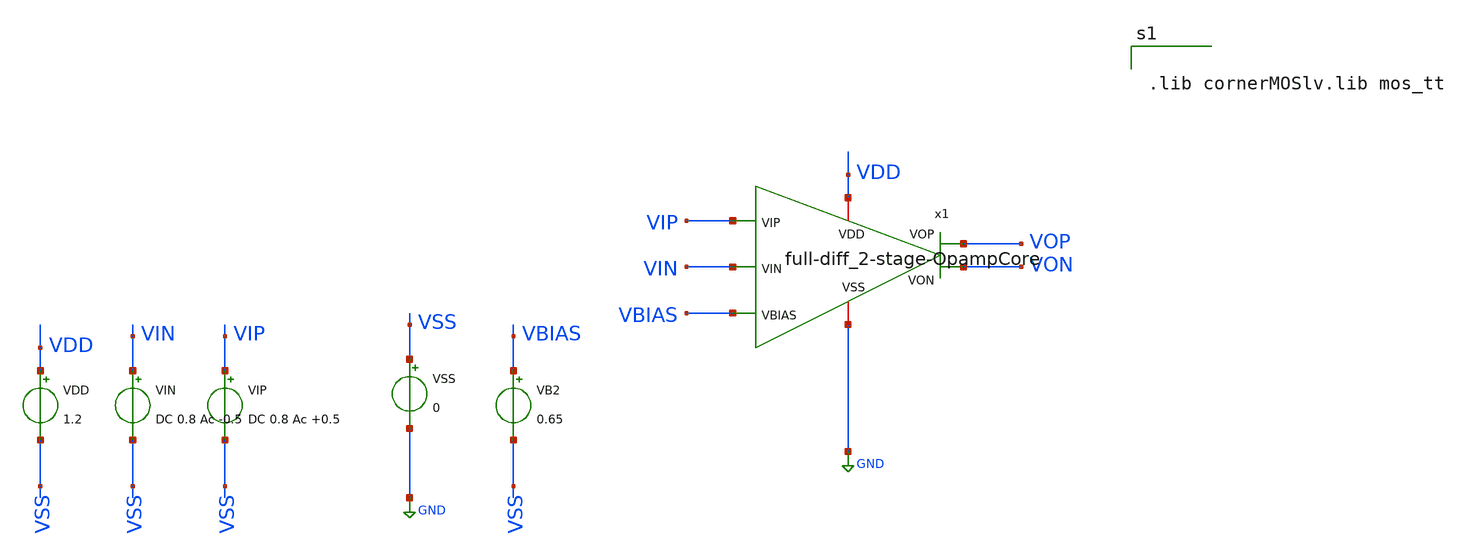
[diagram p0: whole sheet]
** sch_path: BTDay5-Ex/Test-diff_2stageOpampCore.sch
**.subckt Test-diff_2stageOpampCore
VDD VDD VSS 1.2
VIN VIN VSS DC 0.8 Ac -0.5
VIP VIP VSS DC 0.8 Ac +0.5
VSS VSS GND 0
VB2 VBIAS VSS 0.65
x1 VDD VBIAS VOP VON VIP VIN GND full-diff_2-stage-OpampCore
**** begin user architecture code


.lib cornerMOSlv.lib mos_tt




.control
save all
op

* 1. DO CONG SUAT VA DIEM LAM VIEC DC
let power_mw = abs(i(vdd)[0]) * 1.2 * 1000
echo ================= KET QUA DC & CONG SUAT =================
print v(vip) v(vin) v(vbias) v(vop) v(von)
print power_mw

* 2. MO PHONG AC VA TINH TOAN HE SO
ac dec 100 1 10G

let vid = v(vip) - v(vin)
let vod = v(vop) - v(von)
let av = vod / vid
let gain_db = db(av)
let phase_deg = cph(av) * 180 / pi

* Do Open Loop Gain o tan so thap (dang so lan)
let open_loop_gain_times = mag(av[0])

if phase_deg[0] > 90
  let phase_deg = phase_deg - 360
end

* Do tan so cat 0dB va Phase Margin
meas ac f_ug when gain_db=0 fall=1
meas ac phase_at_ug find phase_deg when gain_db=0 fall=1
let phase_margin = 180 + phase_at_ug

echo ================= TONG HOP CHI TIEU EX2 =================
echo 1. Open Loop Gain (Yeu cau: > 3000):
print open_loop_gain_times
echo 2. DC Gain dB (Yeu cau: > 50 dB):
print gain_db[0]
echo 3. Bandwidth GBW f_ug (Yeu cau: > 3 MHz):
print f_ug
echo 4. Phase Margin (Yeu cau: 50 - 60 deg):
print phase_margin
echo 5. Cong suat Power (Yeu cau: < 2 mW):
print power_mw
echo =========================================================

let line_0db = 0 * frequency
let line_m180 = -180 + 0 * frequency

plot gain_db phase_deg line_0db line_m180 xlog ylimit -360 80 title 'Ex2: Fully-Diff OpAmp Open-Loop Frequency Response'
.endc


**** end user architecture code
**.ends

* expanding   symbol:  /foss/designs/BTDay5-Ex/full-diff_2-stage-OpampCore.sym # of pins=7
** sym_path: BTDay5-Ex/full-diff_2-stage-OpampCore.sym
** sch_path: BTDay5-Ex/full-diff_2-stage-OpampCore.sch
.subckt full-diff_2-stage-OpampCore VDD VBIAS VOP VON VIP VIN VSS
*.ipin VIN
*.ipin VIP
*.opin VOP
*.iopin VDD
*.iopin VSS
*.ipin VBIAS
*.opin VON
XM1 net3 VIN net1 VSS sg13_lv_nmos w=4u l=1u ng=1 m=2 mm_ok=1
XM2 net2 VIP net1 VSS sg13_lv_nmos w=4u l=1u ng=1 m=2 mm_ok=1
XM3 net1 VB2 VSS VSS sg13_lv_nmos w=4u l=1u ng=1 m=4 mm_ok=1
XM4 net3 VB1 VDD VDD sg13_lv_pmos w=8u l=1u ng=1 m=2 mm_ok=1
XM7 VB2 VB2 VSS VSS sg13_lv_nmos w=4u l=1u ng=1 m=1 mm_ok=1
XM8 VB2 VBIAS VDD VDD sg13_lv_pmos w=2u l=6u ng=1 m=1 mm_ok=1
XM10 net2 VB1 VDD VDD sg13_lv_pmos w=8u l=1u ng=1 m=2 mm_ok=1
XM5 VOP VB2 VSS VSS sg13_lv_nmos w=4u l=1u ng=1 m=5 mm_ok=1
XM11 VOP net2 VDD VDD sg13_lv_pmos w=4u l=1u ng=1 m=5 mm_ok=1
C2 VOP net4 0.4p m=1
R1 net4 net2 150k m=1
XM9 VON VB2 VSS VSS sg13_lv_nmos w=4u l=1u ng=1 m=5 mm_ok=1
C3 net5 VON 0.4p m=1
R2 net3 net5 150k m=1
XM12 VB1 VB1 VDD VDD sg13_lv_pmos w=8u l=1u ng=1 m=1 mm_ok=1
XM13 VB1 VB2 VSS VSS sg13_lv_nmos w=4u l=1u ng=1 m=1 mm_ok=1
XM6 VON net3 VDD VDD sg13_lv_pmos w=4u l=1u ng=1 m=5 mm_ok=1
.ends

.GLOBAL GND
.end
